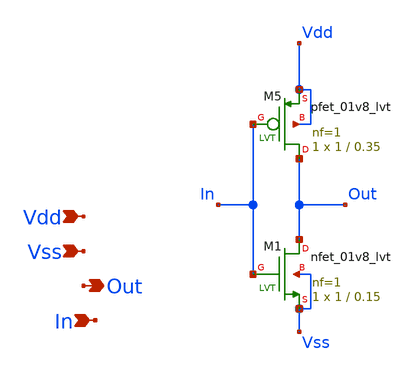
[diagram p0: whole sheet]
** sch_path: tt10-hdl/tt_um_test_commit/xschem/A1_templates/subcircuit_template.sch
**.subckt subcircuit_template Vdd Vss Out In
*.ipin Vdd
*.ipin Vss
*.opin Out
*.ipin In
XM5 Out In Vdd Vdd sky130_fd_pr__pfet_01v8_lvt L=0.35 W=1 nf=1 ad='int((1 + 1)/2) * 1 / 1 * 0.29' as='int((1 + 2)/2) * 1 / 1 * 0.29'
+ pd='2*int((1 + 1)/2) * (1 / 1 + 0.29)' ps='2*int((1 + 2)/2) * (1 / 1 + 0.29)' nrd='0.29 / 1 ' nrs='0.29 / 1 '
+ sa=0 sb=0 sd=0 mult=1 m=1
XM1 Out In Vss Vss sky130_fd_pr__nfet_01v8_lvt L=0.15 W=1 nf=1 ad='int((1 + 1)/2) * 1 / 1 * 0.29' as='int((1 + 2)/2) * 1 / 1 * 0.29'
+ pd='2*int((1 + 1)/2) * (1 / 1 + 0.29)' ps='2*int((1 + 2)/2) * (1 / 1 + 0.29)' nrd='0.29 / 1 ' nrs='0.29 / 1 '
+ sa=0 sb=0 sd=0 mult=1 m=1
**.ends
.end
